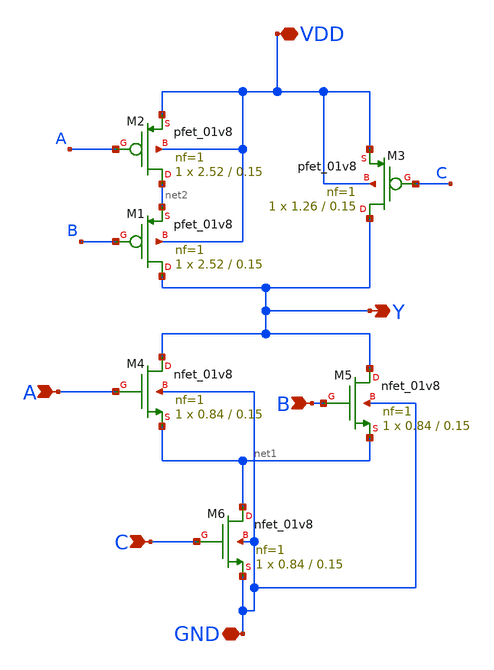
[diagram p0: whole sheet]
** sch_path: cells/OAI3X1/schematic/oai3x1.sch
**.subckt oai3x1 VDD GND A B C Y
*.iopin VDD
*.iopin GND
*.ipin A
*.ipin B
*.ipin C
*.opin Y
XM1 Y B net2 VDD sky130_fd_pr__pfet_01v8 L=0.15 W=2.52 nf=1 ad='int((1 + 1)/2) * 2.52 / 1 * 0.29' as='int((1 + 2)/2) * 2.52 / 1 * 0.29'
+ pd='2*int((1 + 1)/2) * (2.52 / 1 + 0.29)' ps='2*int((1 + 2)/2) * (2.52 / 1 + 0.29)' nrd='0.29 / 2.52 '
+ nrs='0.29 / 2.52 ' sa=0 sb=0 sd=0 mult=1 m=1
XM2 net2 A VDD VDD sky130_fd_pr__pfet_01v8 L=0.15 W=2.52 nf=1 ad='int((1 + 1)/2) * 2.52 / 1 * 0.29' as='int((1 + 2)/2) * 2.52 / 1 * 0.29'
+ pd='2*int((1 + 1)/2) * (2.52 / 1 + 0.29)' ps='2*int((1 + 2)/2) * (2.52 / 1 + 0.29)' nrd='0.29 / 2.52 '
+ nrs='0.29 / 2.52 ' sa=0 sb=0 sd=0 mult=1 m=1
XM3 Y C VDD VDD sky130_fd_pr__pfet_01v8 L=0.15 W=1.26 nf=1 ad='int((1 + 1)/2) * 1.26 / 1 * 0.29' as='int((1 + 2)/2) * 1.26 / 1 * 0.29'
+ pd='2*int((1 + 1)/2) * (1.26 / 1 + 0.29)' ps='2*int((1 + 2)/2) * (1.26 / 1 + 0.29)' nrd='0.29 / 1.26 '
+ nrs='0.29 / 1.26 ' sa=0 sb=0 sd=0 mult=1 m=1
XM4 Y A net1 GND sky130_fd_pr__nfet_01v8 L=0.15 W=0.84 nf=1 ad='int((1 + 1)/2) * 0.84 / 1 * 0.29' as='int((1 + 2)/2) * 0.84 / 1 * 0.29'
+ pd='2*int((1 + 1)/2) * (0.84 / 1 + 0.29)' ps='2*int((1 + 2)/2) * (0.84 / 1 + 0.29)' nrd='0.29 / 0.84 '
+ nrs='0.29 / 0.84 ' sa=0 sb=0 sd=0 mult=1 m=1
XM5 Y B net1 GND sky130_fd_pr__nfet_01v8 L=0.15 W=0.84 nf=1 ad='int((1 + 1)/2) * 0.84 / 1 * 0.29' as='int((1 + 2)/2) * 0.84 / 1 * 0.29'
+ pd='2*int((1 + 1)/2) * (0.84 / 1 + 0.29)' ps='2*int((1 + 2)/2) * (0.84 / 1 + 0.29)' nrd='0.29 / 0.84 '
+ nrs='0.29 / 0.84 ' sa=0 sb=0 sd=0 mult=1 m=1
XM6 net1 C GND GND sky130_fd_pr__nfet_01v8 L=0.15 W=0.84 nf=1 ad='int((1 + 1)/2) * 0.84 / 1 * 0.29' as='int((1 + 2)/2) * 0.84 / 1 * 0.29'
+ pd='2*int((1 + 1)/2) * (0.84 / 1 + 0.29)' ps='2*int((1 + 2)/2) * (0.84 / 1 + 0.29)' nrd='0.29 / 0.84 '
+ nrs='0.29 / 0.84 ' sa=0 sb=0 sd=0 mult=1 m=1
**.ends
.end
